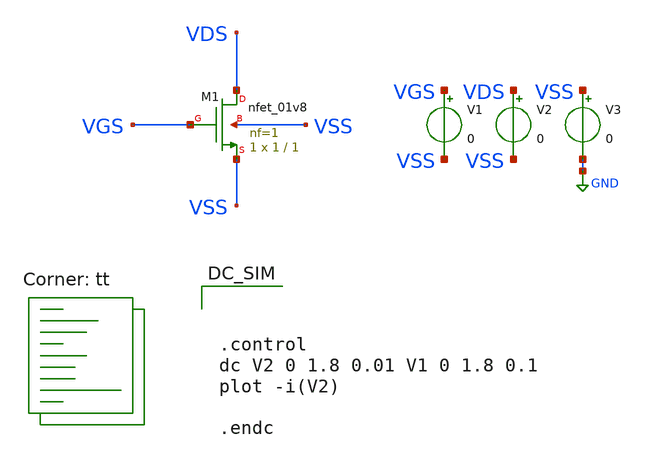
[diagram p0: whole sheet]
** sch_path: designs/libs/core_analog/p-ota/examples/fet-tb/tb_nfet.sch
**.subckt tb_nfet
XM1 VDS VGS VSS VSS sky130_fd_pr__nfet_01v8 L=1 W=1 nf=1 ad='int((nf+1)/2) * W/nf * 0.29' as='int((nf+2)/2) * W/nf * 0.29'
+ pd='2*int((nf+1)/2) * (W/nf + 0.29)' ps='2*int((nf+2)/2) * (W/nf + 0.29)' nrd='0.29 / W' nrs='0.29 / W'
+ sa=0 sb=0 sd=0 mult=1 m=1
V1 VGS VSS 0
V2 VDS VSS 0
V3 VSS GND 0
**** begin user architecture code
.lib $::SKYWATER_MODELS/sky130.lib.spice tt



.control
dc V2 0 1.8 0.01 V1 0 1.8 0.1
plot -i(V2)

.endc

**** end user architecture code
**.ends
.GLOBAL GND
.end
